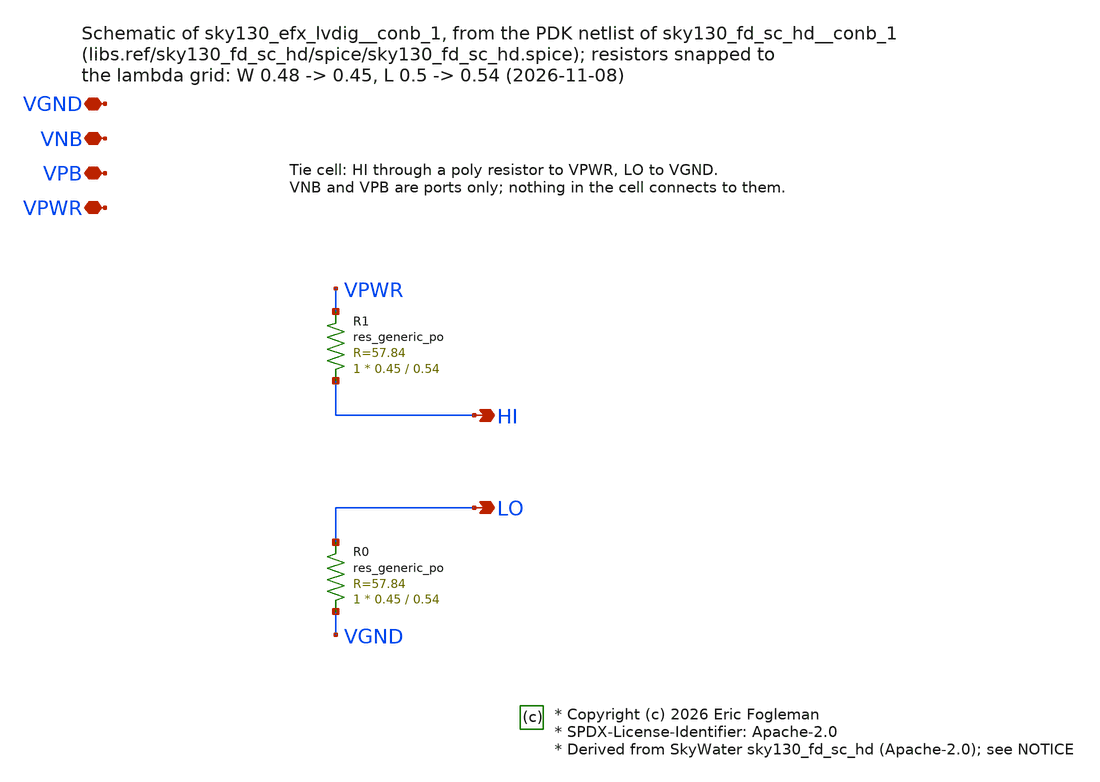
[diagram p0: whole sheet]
** sch_path: xschem/sky130_efx_lvdig__conb_1.sch

* Copyright (c) 2026 Eric Fogleman
* SPDX-License-Identifier: Apache-2.0
* Derived from SkyWater sky130_fd_sc_hd (Apache-2.0); see NOTICE

**.subckt sky130_efx_lvdig__conb_1 VGND VNB VPB VPWR HI LO
*.iopin VGND
*.iopin VNB
*.iopin VPB
*.iopin VPWR
*.opin HI
*.opin LO
XR1 HI VPWR sky130_fd_pr__res_generic_po W=0.45 L=0.54 m=1
XR0 VGND LO sky130_fd_pr__res_generic_po W=0.45 L=0.54 m=1
**.ends
.end
